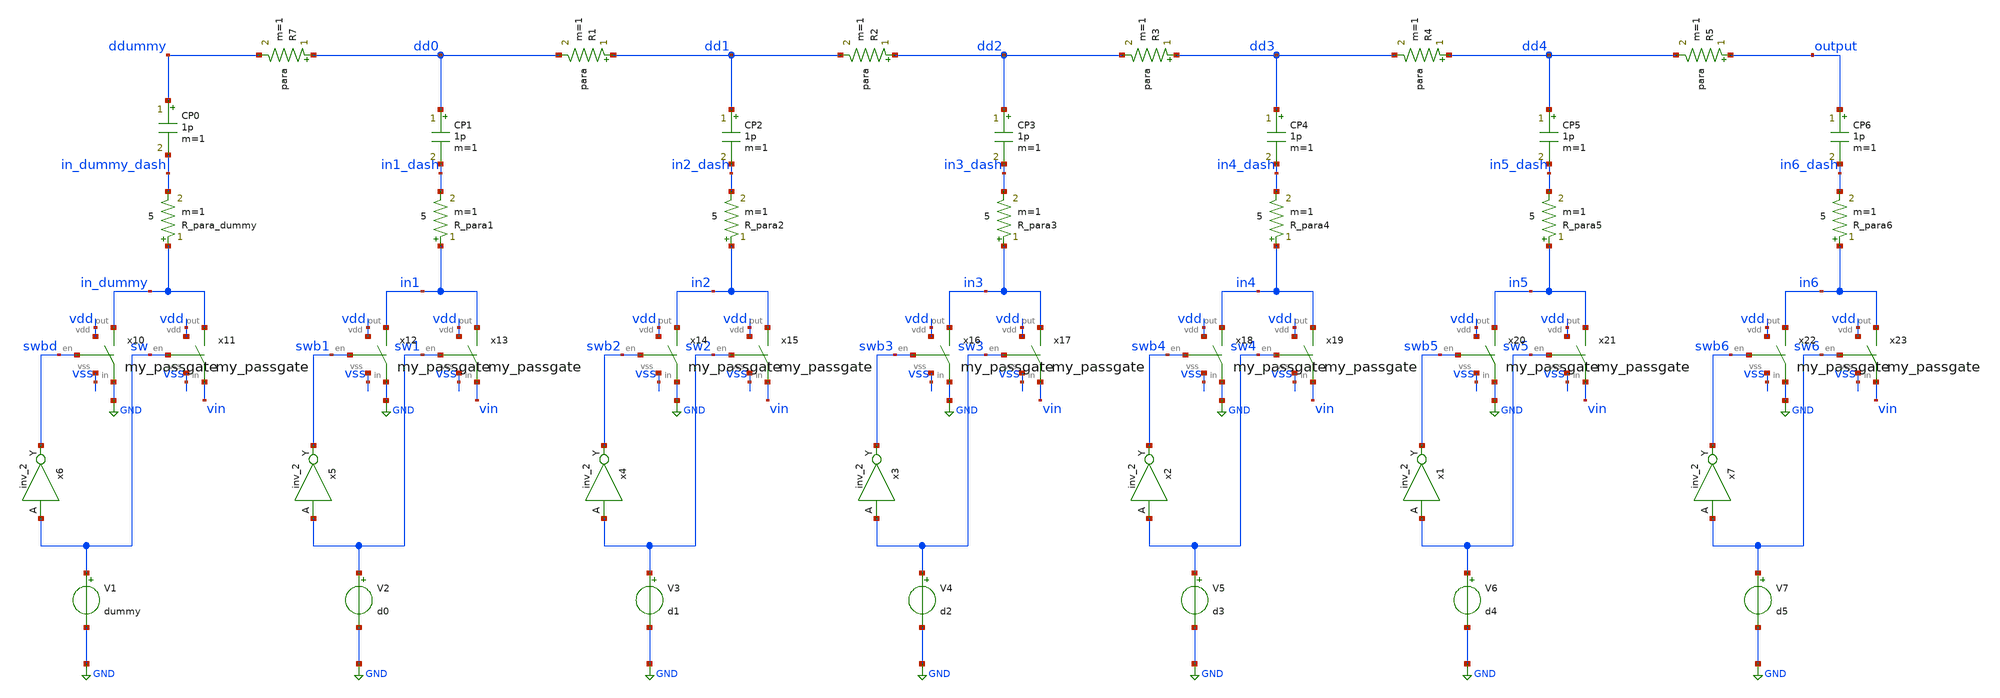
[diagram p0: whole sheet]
** sch_path: xschem/tb/cdac/tb_cdac3.sch
**.subckt tb_cdac3
V1 sw GND dummy
V2 sw1 GND d0
V3 sw2 GND d1
V4 sw3 GND d2
V5 sw4 GND d3
V6 sw5 GND d4
V7 sw6 GND d5
x10 in_dummy swbd vdd GND vss my_passgate
x11 in_dummy sw vdd vin vss my_passgate
x12 in1 swb1 vdd GND vss my_passgate
x13 in1 sw1 vdd vin vss my_passgate
x14 in2 swb2 vdd GND vss my_passgate
x15 in2 sw2 vdd vin vss my_passgate
x16 in3 swb3 vdd GND vss my_passgate
x17 in3 sw3 vdd vin vss my_passgate
x18 in4 swb4 vdd GND vss my_passgate
x19 in4 sw4 vdd vin vss my_passgate
x20 in5 swb5 vdd GND vss my_passgate
x21 in5 sw5 vdd vin vss my_passgate
x22 in6 swb6 vdd GND vss my_passgate
x23 in6 sw6 vdd vin vss my_passgate
x7 sw6 vss vss vdd vdd swb6 sky130_fd_sc_hd__inv_2
x1 sw5 vss vss vdd vdd swb5 sky130_fd_sc_hd__inv_2
x2 sw4 vss vss vdd vdd swb4 sky130_fd_sc_hd__inv_2
x3 sw3 vss vss vdd vdd swb3 sky130_fd_sc_hd__inv_2
x4 sw2 vss vss vdd vdd swb2 sky130_fd_sc_hd__inv_2
x5 sw1 vss vss vdd vdd swb1 sky130_fd_sc_hd__inv_2
x6 sw vss vss vdd vdd swbd sky130_fd_sc_hd__inv_2
R7 dd0 ddummy para m=1
R1 dd1 dd0 para m=1
R2 dd2 dd1 para m=1
R3 dd3 dd2 para m=1
R4 dd4 dd3 para m=1
R5 output dd4 para m=1
R_para_dummy in_dummy in_dummy_dash 5 m=1
R_para1 in1 in1_dash 5 m=1
R_para2 in2 in2_dash 5 m=1
R_para3 in3 in3_dash 5 m=1
R_para4 in4 in4_dash 5 m=1
R_para5 in5 in5_dash 5 m=1
R_para6 in6 in6_dash 5 m=1
CP0 ddummy in_dummy_dash 1p m=1
CP1 dd0 in1_dash 1p m=1
CP2 dd1 in2_dash 1p m=1
CP3 dd2 in3_dash 1p m=1
CP4 dd3 in4_dash 1p m=1
CP5 dd4 in5_dash 1p m=1
CP6 output in6_dash 1p m=1
**** begin user architecture code
 * FET CORNERS
.include $::SKYWATER_MODELS/models/corners/tt.spice
*.include $::SKYWATER_MODELS/corners/ff.spice
*.include $::SKYWATER_MODELS/corners/ss.spice
*.include $::SKYWATER_MODELS/corners/sf.spice
*.include $::SKYWATER_MODELS/corners/fs.spice

* TT + R + C
*.include $::SKYWATER_MODELS/corners/tt_rmax_cmax.spice
*.include $::SKYWATER_MODELS/corners/tt_rmin_cmin.spice
*.include $::SKYWATER_MODELS/corners/tt_rmax_cmin.spice
*.include $::SKYWATER_MODELS/corners/tt_rmin_cmax.spice

* FF + R + C
*.include $::SKYWATER_MODELS/corners/ff_rmax_cmax.spice
*.include $::SKYWATER_MODELS/corners/ff_rmin_cmin.spice
*.include $::SKYWATER_MODELS/corners/ff_rmax_cmin.spice
*.include $::SKYWATER_MODELS/corners/ff_rmin_cmax.spice


* SS + R + C
*.include $::SKYWATER_MODELS/corners/ss_rmax_cmax.spice
*.include $::SKYWATER_MODELS/corners/ss_rmin_cmin.spice
*.include $::SKYWATER_MODELS/corners/ss_rmax_cmin.spice
*.include $::SKYWATER_MODELS/corners/ss_rmin_cmax.spice

* SF + R + C
*.include $::SKYWATER_MODELS/corners/sf_rmax_cmax.spice
*.include $::SKYWATER_MODELS/corners/sf_rmin_cmin.spice
*.include $::SKYWATER_MODELS/corners/sf_rmax_cmin.spice
*.include $::SKYWATER_MODELS/corners/sf_rmin_cmax.spice

* FS + R + C
*.include $::SKYWATER_MODELS/corners/fs_rmax_cmax.spice
*.include $::SKYWATER_MODELS/corners/fs_rmin_cmin.spice
*.include $::SKYWATER_MODELS/corners/fs_rmax_cmin.spice
*.include $::SKYWATER_MODELS/corners/fs_rmin_cmax.spice



.option wnflag=1
.option plotwinsize=0
Vin vin 0 dc PULSE(0 1 0 12.8u 0 0.2u 13u)
*Vin vin 0 1.8
VDD vdd 0 1.8
VSS vss 0 0

.param dummy=0
.param d5=1
.param d4=0
.param d3=0
.param d2=0
.param d1=0
.param d0=0
.param para=5

.control
save all
tran 1u 13u

meas tran output find v(d5) at=13u

wrdata out output
print output
.endc




.include $::SKYWATER_STDCELLS/cells/inv/sky130_fd_sc_hd__inv_2.spice
**** end user architecture code
**.ends

* expanding   symbol:  switches/my_passgate.sym # of pins=5
** sym_path: xschem/switches/my_passgate.sym
** sch_path: xschem/switches/my_passgate.sch
.subckt my_passgate out en vdd in vss
*.iopin out
*.ipin en
*.iopin vss
*.iopin vdd
*.iopin in
x2 vdd en enb vss inv_lvt
x1 vdd enb en_buf vss inv_lvt
XMSN out en_buf in vss sky130_fd_pr__nfet_01v8 L=0.5 W=1 nf=1 ad='int((nf+1)/2) * W/nf * 0.29' as='int((nf+2)/2) * W/nf * 0.29'
+ pd='2*int((nf+1)/2) * (W/nf + 0.29)' ps='2*int((nf+2)/2) * (W/nf + 0.29)' nrd='0.29 / W' nrs='0.29 / W'
+ sa=0 sb=0 sd=0 mult=1 m=1
XMSP in enb out vdd sky130_fd_pr__pfet_01v8 L=0.5 W=1 nf=1 ad='int((nf+1)/2) * W/nf * 0.29' as='int((nf+2)/2) * W/nf * 0.29'
+ pd='2*int((nf+1)/2) * (W/nf + 0.29)' ps='2*int((nf+2)/2) * (W/nf + 0.29)' nrd='0.29 / W' nrs='0.29 / W'
+ sa=0 sb=0 sd=0 mult=1 m=1
.ends


* expanding   symbol:  logic/inv_lvt.sym # of pins=4
** sym_path: logic/inv_lvt.sym
** sch_path: logic/inv_lvt.sch
.subckt inv_lvt vdd in out vss
*.iopin vdd
*.iopin vss
*.ipin in
*.opin out
XM1 out in vss vss sky130_fd_pr__nfet_01v8_lvt L=0.4 W=1 nf=1 ad='int((nf+1)/2) * W/nf * 0.29' as='int((nf+2)/2) * W/nf * 0.29'
+ pd='2*int((nf+1)/2) * (W/nf + 0.29)' ps='2*int((nf+2)/2) * (W/nf + 0.29)' nrd='0.29 / W' nrs='0.29 / W'
+ sa=0 sb=0 sd=0 mult=1 m=1
XM2 out in vdd vdd sky130_fd_pr__pfet_01v8_lvt L=0.4 W=1 nf=1 ad='int((nf+1)/2) * W/nf * 0.29' as='int((nf+2)/2) * W/nf * 0.29'
+ pd='2*int((nf+1)/2) * (W/nf + 0.29)' ps='2*int((nf+2)/2) * (W/nf + 0.29)' nrd='0.29 / W' nrs='0.29 / W'
+ sa=0 sb=0 sd=0 mult=1 m=1
.ends

.GLOBAL GND
.end
